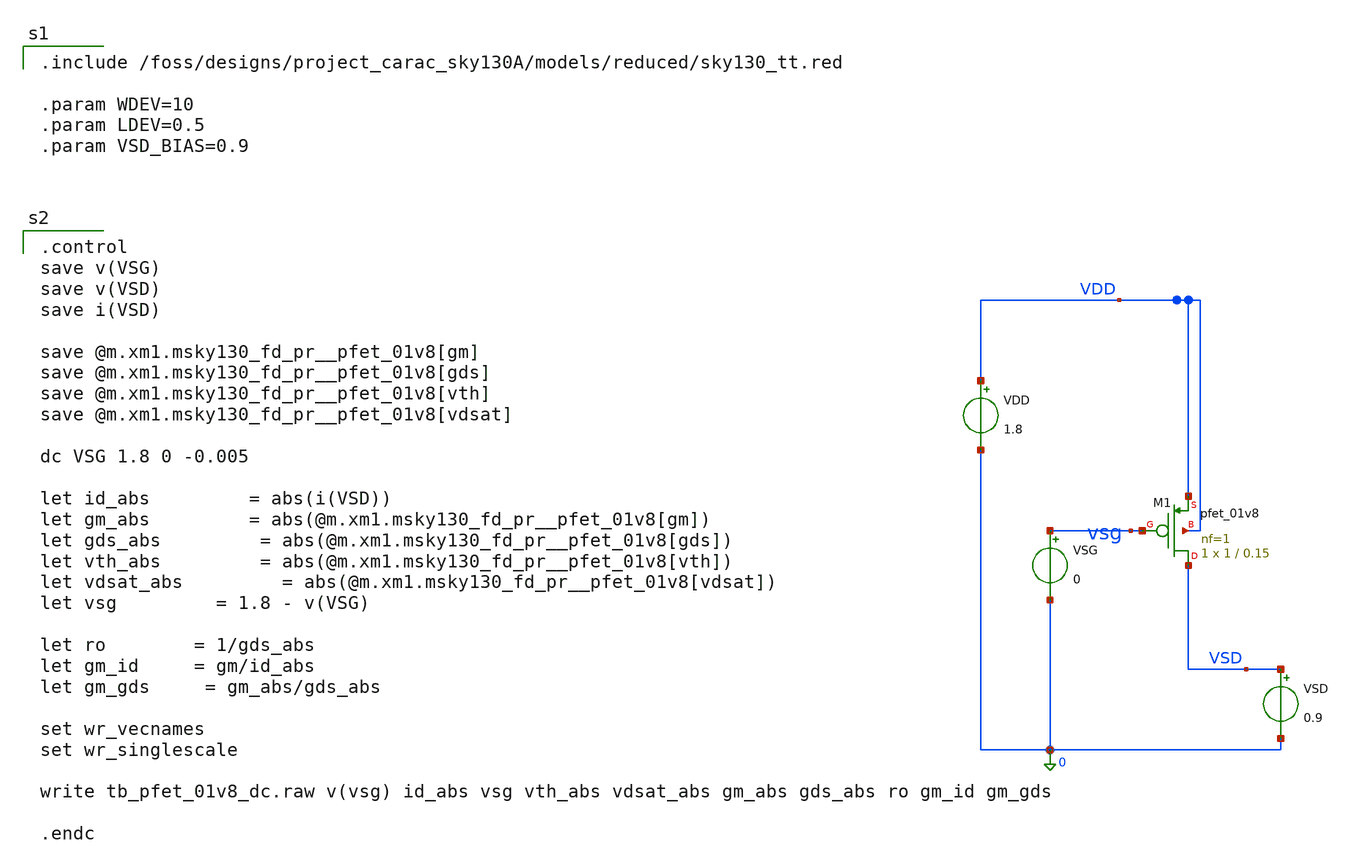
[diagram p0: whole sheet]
** sch_path: dfii/project_carac_sky130A_sim/tb_pfet_01v8_dc.sch
* Copyright 2021 Stefan Frederik Schippers
* Licensed under the Apache License, Version 2.0 (the "License");
* you may not use this file except in compliance with the License.
* You may obtain a copy of the License at
* https://www.apache.org/licenses/LICENSE-2.0
* Unless required by applicable law or agreed to in writing, software
* distributed under the License is distributed on an "AS IS" BASIS,
* WITHOUT WARRANTIES OR CONDITIONS OF ANY KIND, either express or implied.
* See the License for the specific language governing permissions and
* limitations under the License.

.include /foss/designs/project_carac_sky130A/models/reduced/sky130_tt.red

.param WDEV=10
.param LDEV=0.5
.param VSD_BIAS=0.9



**.subckt tb_pfet_01v8_dc
VSG vsg 0 0
VSD VSD 0 0.9
.save i(vsd)
XM1 VSD vsg VDD VDD sky130_fd_pr__pfet_01v8 L=0.15 W=1 nf=1 ad='int((1 + 1)/2) * 1 / 1 * 0.29' as='int((1 + 2)/2) * 1 / 1 * 0.29'
+ pd='2*int((1 + 1)/2) * (1 / 1 + 0.29)' ps='2*int((1 + 2)/2) * (1 / 1 + 0.29)' nrd='0.29 / 1 ' nrs='0.29 / 1 '
+ sa=0 sb=0 sd=0 mult=1 m=1
VDD VDD 0 1.8
**.ends
**** begin user architecture code

.control
save v(VSG)
save v(VSD)
save i(VSD)

save @m.xm1.msky130_fd_pr__pfet_01v8[gm]
save @m.xm1.msky130_fd_pr__pfet_01v8[gds]
save @m.xm1.msky130_fd_pr__pfet_01v8[vth]
save @m.xm1.msky130_fd_pr__pfet_01v8[vdsat]

dc VSG 1.8 0 -0.005

let id_abs 		= abs(i(VSD))
let gm_abs 		= abs(@m.xm1.msky130_fd_pr__pfet_01v8[gm])
let gds_abs 		= abs(@m.xm1.msky130_fd_pr__pfet_01v8[gds])
let vth_abs 		= abs(@m.xm1.msky130_fd_pr__pfet_01v8[vth])
let vdsat_abs 		= abs(@m.xm1.msky130_fd_pr__pfet_01v8[vdsat])
let vsg 		= 1.8 - v(VSG)

let ro		= 1/gds_abs
let gm_id 	= gm/id_abs
let gm_gds 	= gm_abs/gds_abs

set wr_vecnames
set wr_singlescale

write tb_pfet_01v8_dc.raw v(vsg) id_abs vsg vth_abs vdsat_abs gm_abs gds_abs ro gm_id gm_gds

.endc

**** end user architecture code
.end
